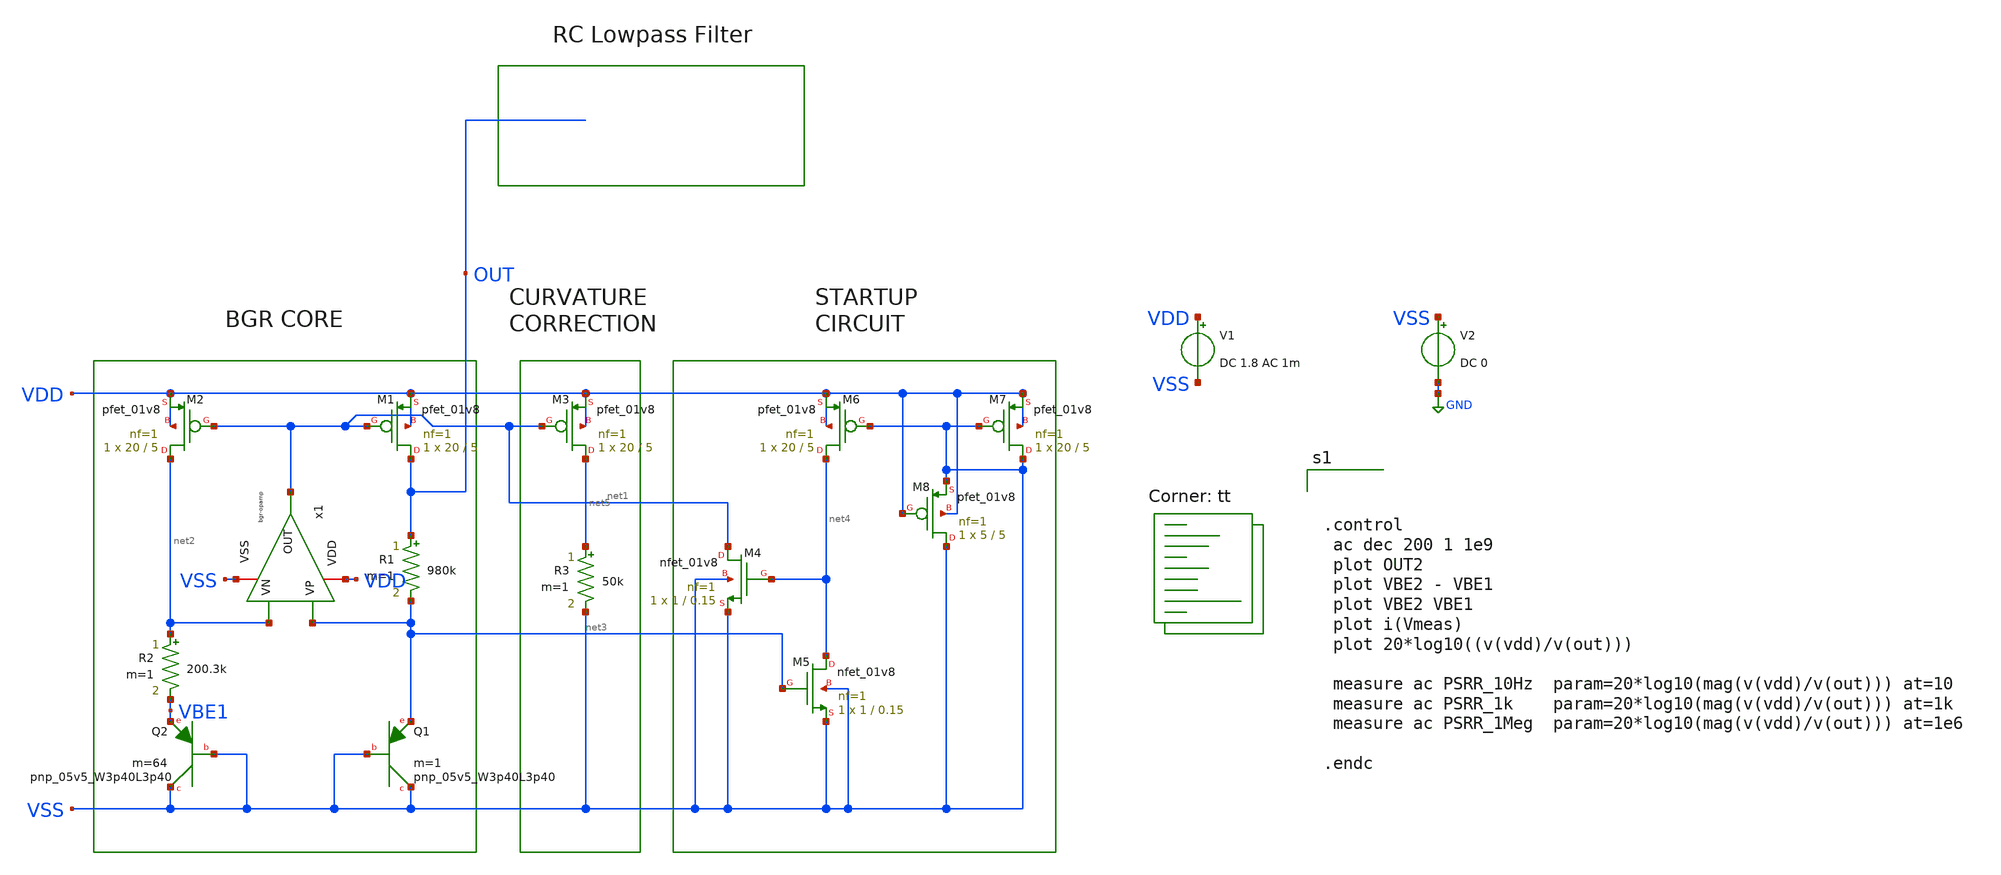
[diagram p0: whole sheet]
** sch_path: bandgap/bgr2-ac.sch
**.subckt bgr2-ac
x1 VDD net1 net3 net2 VSS bgr-opamp
XM1 OUT net1 VDD VDD sky130_fd_pr__pfet_01v8 L=5 W=20 nf=1 ad='int((nf+1)/2) * W/nf * 0.29' as='int((nf+2)/2) * W/nf * 0.29'
+ pd='2*int((nf+1)/2) * (W/nf + 0.29)' ps='2*int((nf+2)/2) * (W/nf + 0.29)' nrd='0.29 / W' nrs='0.29 / W'
+ sa=0 sb=0 sd=0 mult=1 m=1
XM2 net2 net1 VDD VDD sky130_fd_pr__pfet_01v8 L=5 W=20 nf=1 ad='int((nf+1)/2) * W/nf * 0.29' as='int((nf+2)/2) * W/nf * 0.29'
+ pd='2*int((nf+1)/2) * (W/nf + 0.29)' ps='2*int((nf+2)/2) * (W/nf + 0.29)' nrd='0.29 / W' nrs='0.29 / W'
+ sa=0 sb=0 sd=0 mult=1 m=1
R1 OUT net3 980k m=1
R2 net2 VBE1 200.3k m=1
XQ1 VSS VSS net3 sky130_fd_pr__pnp_05v5_W3p40L3p40 m=1
XQ2 VSS VSS VBE1 sky130_fd_pr__pnp_05v5_W3p40L3p40 m=64
V1 VDD VSS DC 1.8 AC 1m
V2 VSS GND DC 0
XM3 net5 net1 VDD VDD sky130_fd_pr__pfet_01v8 L=5 W=20 nf=1 ad='int((nf+1)/2) * W/nf * 0.29' as='int((nf+2)/2) * W/nf * 0.29'
+ pd='2*int((nf+1)/2) * (W/nf + 0.29)' ps='2*int((nf+2)/2) * (W/nf + 0.29)' nrd='0.29 / W' nrs='0.29 / W'
+ sa=0 sb=0 sd=0 mult=1 m=1
R3 net5 VSS 50k m=1
XM4 net1 net4 VSS VSS sky130_fd_pr__nfet_01v8 L=0.15 W=1 nf=1 ad='int((nf+1)/2) * W/nf * 0.29' as='int((nf+2)/2) * W/nf * 0.29'
+ pd='2*int((nf+1)/2) * (W/nf + 0.29)' ps='2*int((nf+2)/2) * (W/nf + 0.29)' nrd='0.29 / W' nrs='0.29 / W'
+ sa=0 sb=0 sd=0 mult=1 m=1
XM5 net4 net3 VSS VSS sky130_fd_pr__nfet_01v8 L=0.15 W=1 nf=1 ad='int((nf+1)/2) * W/nf * 0.29' as='int((nf+2)/2) * W/nf * 0.29'
+ pd='2*int((nf+1)/2) * (W/nf + 0.29)' ps='2*int((nf+2)/2) * (W/nf + 0.29)' nrd='0.29 / W' nrs='0.29 / W'
+ sa=0 sb=0 sd=0 mult=1 m=1
XM6 net4 VSS VDD VDD sky130_fd_pr__pfet_01v8 L=5 W=20 nf=1 ad='int((nf+1)/2) * W/nf * 0.29' as='int((nf+2)/2) * W/nf * 0.29'
+ pd='2*int((nf+1)/2) * (W/nf + 0.29)' ps='2*int((nf+2)/2) * (W/nf + 0.29)' nrd='0.29 / W' nrs='0.29 / W'
+ sa=0 sb=0 sd=0 mult=1 m=1
XM7 VSS VSS VDD VDD sky130_fd_pr__pfet_01v8 L=5 W=20 nf=1 ad='int((nf+1)/2) * W/nf * 0.29' as='int((nf+2)/2) * W/nf * 0.29'
+ pd='2*int((nf+1)/2) * (W/nf + 0.29)' ps='2*int((nf+2)/2) * (W/nf + 0.29)' nrd='0.29 / W' nrs='0.29 / W'
+ sa=0 sb=0 sd=0 mult=1 m=1
XM8 VSS VDD VSS VDD sky130_fd_pr__pfet_01v8 L=5 W=5 nf=1 ad='int((nf+1)/2) * W/nf * 0.29' as='int((nf+2)/2) * W/nf * 0.29'
+ pd='2*int((nf+1)/2) * (W/nf + 0.29)' ps='2*int((nf+2)/2) * (W/nf + 0.29)' nrd='0.29 / W' nrs='0.29 / W'
+ sa=0 sb=0 sd=0 mult=1 m=1
**** begin user architecture code
.lib $::SKYWATER_MODELS/sky130.lib.spice tt



.control
 ac dec 200 1 1e9
 plot OUT2
 plot VBE2 - VBE1
 plot VBE2 VBE1
 plot i(Vmeas)
 plot 20*log10((v(vdd)/v(out)))

 measure ac PSRR_10Hz  param=20*log10(mag(v(vdd)/v(out))) at=10
 measure ac PSRR_1k    param=20*log10(mag(v(vdd)/v(out))) at=1k
 measure ac PSRR_1Meg  param=20*log10(mag(v(vdd)/v(out))) at=1e6

.endc


**** end user architecture code
**.ends
.GLOBAL GND
.end
